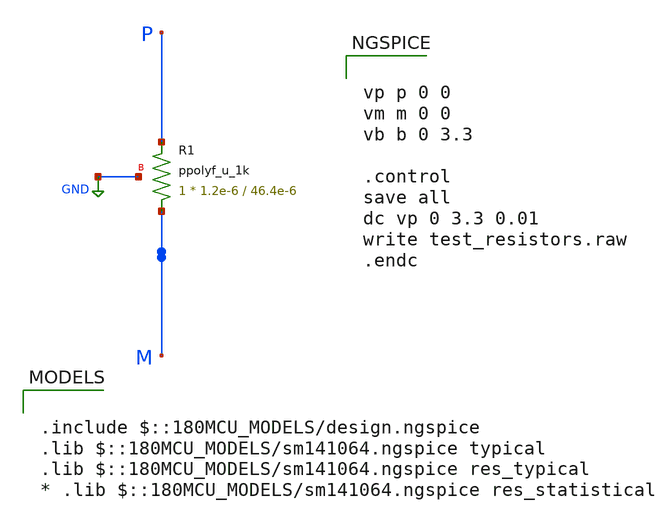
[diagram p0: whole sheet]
** sch_path: Voltage_Reference/LDO/test_resistors.sch
**.subckt test_resistors
XR1 M P GND ppolyf_u_1k r_width=1.2e-6 r_length=46.4e-6 m=1
**** begin user architecture code

.include $::180MCU_MODELS/design.ngspice
.lib $::180MCU_MODELS/sm141064.ngspice typical
.lib $::180MCU_MODELS/sm141064.ngspice res_typical
* .lib $::180MCU_MODELS/sm141064.ngspice res_statistical



vp p 0 0
vm m 0 0
vb b 0 3.3

.control
save all
dc vp 0 3.3 0.01
write test_resistors.raw
.endc


**** end user architecture code
**.ends
.GLOBAL GND
.end
